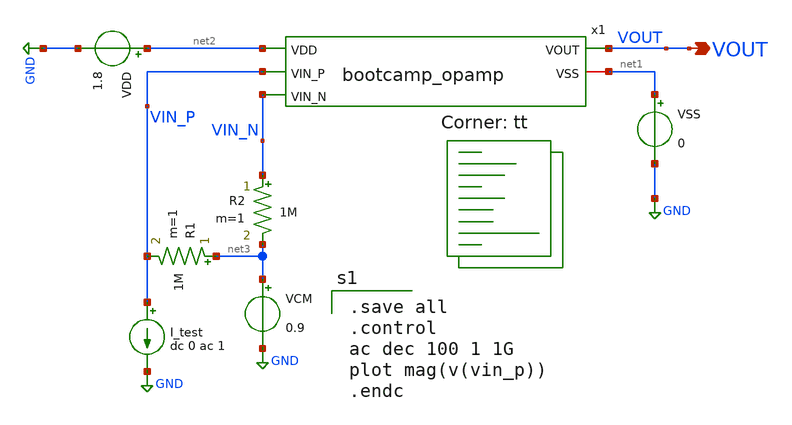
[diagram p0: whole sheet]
** sch_path: analog/build/schematic/tb_impedance.sch
**.subckt tb_impedance VOUT
*.opin VOUT
x1 net2 VOUT VIN_P VIN_N net1 bootcamp_opamp
VSS net1 GND 0
VDD net2 GND 1.8
I_test VIN_P GND dc 0 ac 1
VCM net3 GND 0.9
R1 net3 VIN_P 1M m=1
R2 VIN_N net3 1M m=1
**** begin user architecture code

.save all
.control
ac dec 100 1 1G
plot mag(v(vin_p))
.endc

.lib $::SKYWATER_MODELS/sky130.lib.spice tt
**** end user architecture code
**.ends

* expanding   symbol:  bootcamp_opamp.sym # of pins=5
** sym_path: analog/schematics/bootcamp_opamp.sym
** sch_path: analog/schematics/bootcamp_opamp.sch
.subckt bootcamp_opamp VDD VOUT VIN_P VIN_N VSS
*.ipin VIN_P
*.ipin VIN_N
*.iopin VSS
*.opin VOUT
*.ipin VDD
XM1 net1 net1 VDD VDD sky130_fd_pr__pfet_01v8 L=0.5 W=10 nf=1 ad='int((nf+1)/2) * W/nf * 0.29' as='int((nf+2)/2) * W/nf * 0.29'
+ pd='2*int((nf+1)/2) * (W/nf + 0.29)' ps='2*int((nf+2)/2) * (W/nf + 0.29)' nrd='0.29 / W' nrs='0.29 / W'
+ sa=0 sb=0 sd=0 mult=1 m=1
XM2 VOUT net1 VDD VDD sky130_fd_pr__pfet_01v8 L=0.5 W=10 nf=1 ad='int((nf+1)/2) * W/nf * 0.29' as='int((nf+2)/2) * W/nf * 0.29'
+ pd='2*int((nf+1)/2) * (W/nf + 0.29)' ps='2*int((nf+2)/2) * (W/nf + 0.29)' nrd='0.29 / W' nrs='0.29 / W'
+ sa=0 sb=0 sd=0 mult=1 m=1
XM3 VOUT VOUT VDD VDD sky130_fd_pr__pfet_01v8 L=0.5 W=10 nf=1 ad='int((nf+1)/2) * W/nf * 0.29' as='int((nf+2)/2) * W/nf * 0.29'
+ pd='2*int((nf+1)/2) * (W/nf + 0.29)' ps='2*int((nf+2)/2) * (W/nf + 0.29)' nrd='0.29 / W' nrs='0.29 / W'
+ sa=0 sb=0 sd=0 mult=1 m=1
XM4 net1 VIN_P net2 VSS sky130_fd_pr__nfet_01v8 L=0.5 W=16 nf=1 ad='int((nf+1)/2) * W/nf * 0.29' as='int((nf+2)/2) * W/nf * 0.29'
+ pd='2*int((nf+1)/2) * (W/nf + 0.29)' ps='2*int((nf+2)/2) * (W/nf + 0.29)' nrd='0.29 / W' nrs='0.29 / W'
+ sa=0 sb=0 sd=0 mult=1 m=1
XM5 VOUT VIN_N net2 VSS sky130_fd_pr__nfet_01v8 L=0.5 W=16 nf=1 ad='int((nf+1)/2) * W/nf * 0.29' as='int((nf+2)/2) * W/nf * 0.29'
+ pd='2*int((nf+1)/2) * (W/nf + 0.29)' ps='2*int((nf+2)/2) * (W/nf + 0.29)' nrd='0.29 / W' nrs='0.29 / W'
+ sa=0 sb=0 sd=0 mult=1 m=1
XM6 net2 net3 VSS VSS sky130_fd_pr__nfet_01v8 L=0.8 W=4 nf=1 ad='int((nf+1)/2) * W/nf * 0.29' as='int((nf+2)/2) * W/nf * 0.29'
+ pd='2*int((nf+1)/2) * (W/nf + 0.29)' ps='2*int((nf+2)/2) * (W/nf + 0.29)' nrd='0.29 / W' nrs='0.29 / W'
+ sa=0 sb=0 sd=0 mult=1 m=1
XM7 net3 net3 VSS VSS sky130_fd_pr__nfet_01v8 L=0.8 W=4 nf=1 ad='int((nf+1)/2) * W/nf * 0.29' as='int((nf+2)/2) * W/nf * 0.29'
+ pd='2*int((nf+1)/2) * (W/nf + 0.29)' ps='2*int((nf+2)/2) * (W/nf + 0.29)' nrd='0.29 / W' nrs='0.29 / W'
+ sa=0 sb=0 sd=0 mult=1 m=1
XM8 VOUT VSS VSS VSS sky130_fd_pr__nfet_01v8 L=0.8 W=4 nf=1 ad='int((nf+1)/2) * W/nf * 0.29' as='int((nf+2)/2) * W/nf * 0.29'
+ pd='2*int((nf+1)/2) * (W/nf + 0.29)' ps='2*int((nf+2)/2) * (W/nf + 0.29)' nrd='0.29 / W' nrs='0.29 / W'
+ sa=0 sb=0 sd=0 mult=1 m=1
XC1 VOUT VSS sky130_fd_pr__cap_mim_m3_1 W=1 L=1 MF=1 m=1
R2 net3 VDD sky130_fd_pr__res_generic_m1 W=1 L=1 m=1
.ends

.GLOBAL GND
.end
